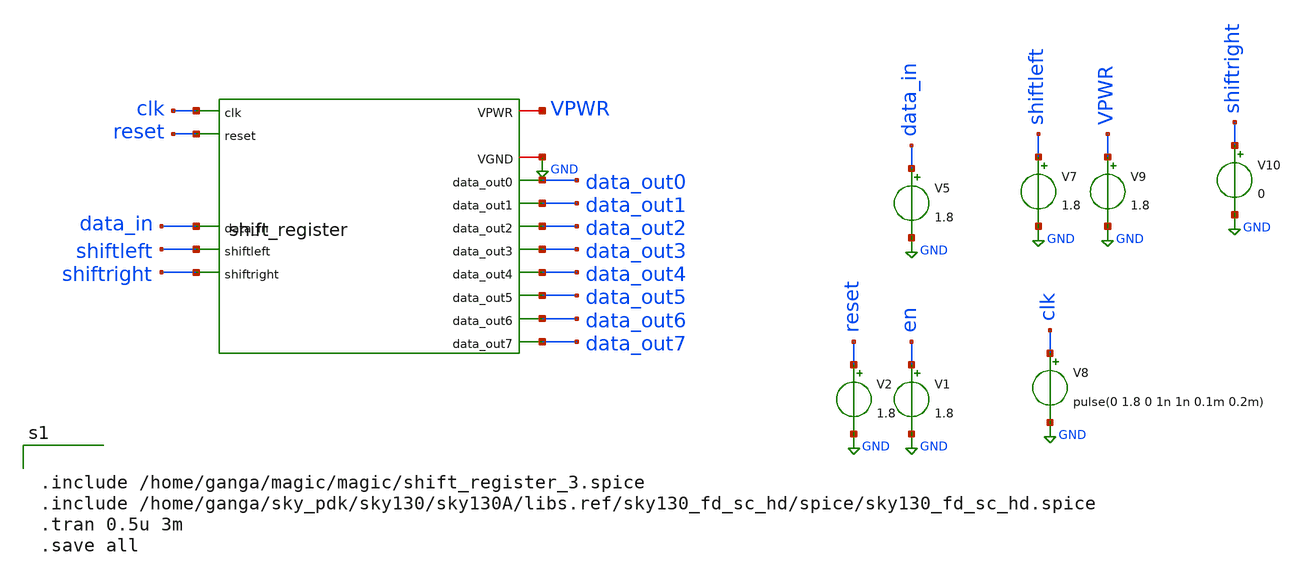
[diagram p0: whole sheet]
** sch_path: xschem/xschemfiles/shiftreg_new.sch
**.subckt shiftreg_new
V2 reset GND 1.8
V1 en GND 1.8
V5 data_in GND 1.8
V7 shiftleft GND 1.8
V8 clk GND pulse(0 1.8 0 1n 1n 0.1m 0.2m)
V9 VPWR GND 1.8
V10 shiftright GND 0
x1 GND VPWR clk data_in data_out0 data_out1 data_out2 data_out3 data_out4 data_out5 data_out6
+ data_out7 reset shiftleft shiftright shift_register
**** begin user architecture code

** opencircuitdesign pdks install
.lib $::SKYWATER_MODELS/sky130.lib.spice tt




.include /home/ganga/magic/magic/shift_register_3.spice
.include /home/ganga/sky_pdk/sky130/sky130A/libs.ref/sky130_fd_sc_hd/spice/sky130_fd_sc_hd.spice
.tran 0.5u 3m
.save all


**** end user architecture code
**.ends
.GLOBAL GND
.end
